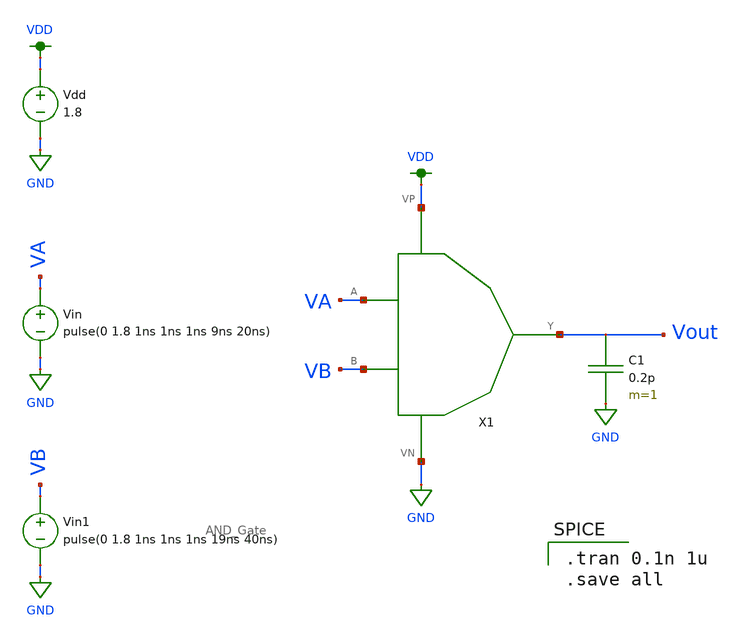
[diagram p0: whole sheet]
** sch_path: Mini_Project_1/Schematic/AND_Top_Level.sch
**.subckt AND_Top_Level
Vdd VDD GND 1.8
Vin VA GND pulse(0 1.8 1ns 1ns 1ns 9ns 20ns)
X1 VB VA Vout VDD GND AND_Gate
Vin1 VB GND pulse(0 1.8 1ns 1ns 1ns 19ns 40ns)
C1 Vout GND 0.2p m=1
**** begin user architecture code

.option wnflag=1
.lib ~/skywater/skywater-pdk/libraries/sky130_fd_pr_ngspice/latest/models/sky130.lib.spice tt


.tran 0.1n 1u
.save all

**** end user architecture code
**.ends
.GLOBAL VDD
.GLOBAL GND
.end
